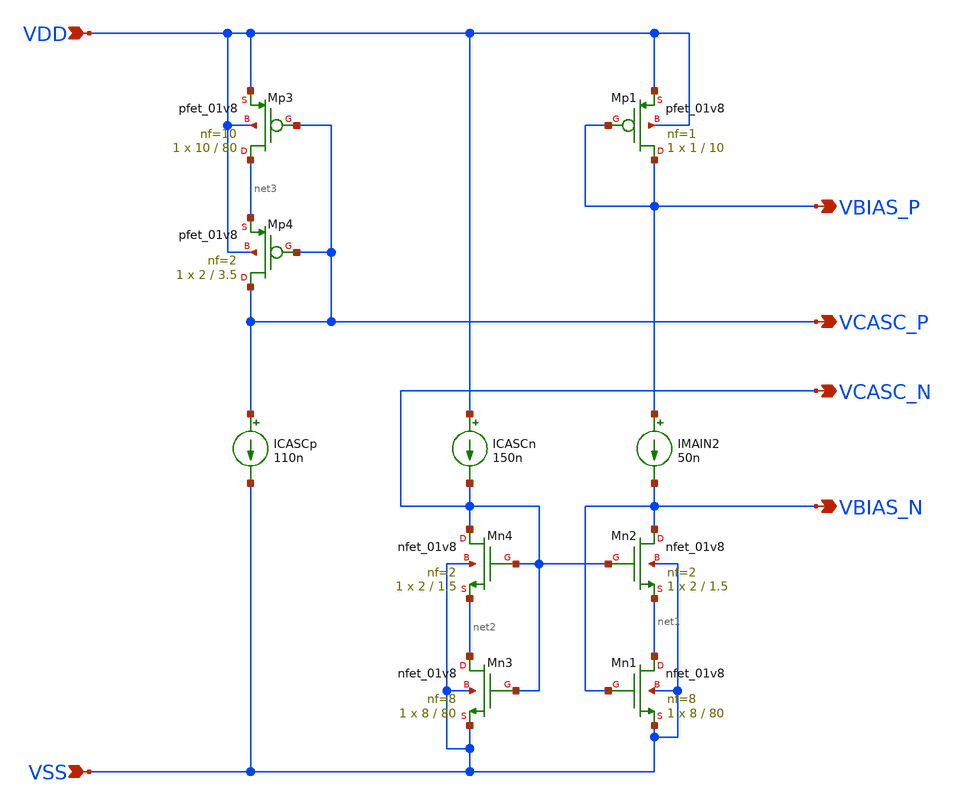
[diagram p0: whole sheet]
** sch_path: circuit-level/xschem/aux-amp/amp_gm_boost_bias_2.sch
**.subckt amp_gm_boost_bias_2 VBIAS_P VSS VDD VBIAS_N VCASC_N VCASC_P
*.opin VBIAS_P
*.ipin VSS
*.ipin VDD
*.opin VBIAS_N
*.opin VCASC_N
*.opin VCASC_P
XMn2 VBIAS_N VCASC_N net1 VSS sky130_fd_pr__nfet_01v8 L=1.5 W=2 nf=2 ad='int((nf+1)/2) * W/nf * 0.29'
+ as='int((nf+2)/2) * W/nf * 0.29' pd='2*int((nf+1)/2) * (W/nf + 0.29)' ps='2*int((nf+2)/2) * (W/nf + 0.29)'
+ nrd='0.29 / W' nrs='0.29 / W' sa=0 sb=0 sd=0 mult=1 m=1
XMn4 VCASC_N VCASC_N net2 VSS sky130_fd_pr__nfet_01v8 L=1.5 W=2 nf=2 ad='int((nf+1)/2) * W/nf * 0.29'
+ as='int((nf+2)/2) * W/nf * 0.29' pd='2*int((nf+1)/2) * (W/nf + 0.29)' ps='2*int((nf+2)/2) * (W/nf + 0.29)'
+ nrd='0.29 / W' nrs='0.29 / W' sa=0 sb=0 sd=0 mult=1 m=1
ICASCn VDD VCASC_N 150n
XMn1 net1 VBIAS_N VSS VSS sky130_fd_pr__nfet_01v8 L=80 W=8 nf=8 ad='int((nf+1)/2) * W/nf * 0.29' as='int((nf+2)/2) * W/nf * 0.29'
+ pd='2*int((nf+1)/2) * (W/nf + 0.29)' ps='2*int((nf+2)/2) * (W/nf + 0.29)' nrd='0.29 / W' nrs='0.29 / W'
+ sa=0 sb=0 sd=0 mult=1 m=1
IMAIN2 VBIAS_P VBIAS_N 50n
XMn3 net2 VCASC_N VSS VSS sky130_fd_pr__nfet_01v8 L=80 W=8 nf=8 ad='int((nf+1)/2) * W/nf * 0.29' as='int((nf+2)/2) * W/nf * 0.29'
+ pd='2*int((nf+1)/2) * (W/nf + 0.29)' ps='2*int((nf+2)/2) * (W/nf + 0.29)' nrd='0.29 / W' nrs='0.29 / W'
+ sa=0 sb=0 sd=0 mult=1 m=1
XMp1 VBIAS_P VBIAS_P VDD VDD sky130_fd_pr__pfet_01v8 L=10 W=1 nf=1 ad='int((nf+1)/2) * W/nf * 0.29' as='int((nf+2)/2) * W/nf * 0.29'
+ pd='2*int((nf+1)/2) * (W/nf + 0.29)' ps='2*int((nf+2)/2) * (W/nf + 0.29)' nrd='0.29 / W' nrs='0.29 / W'
+ sa=0 sb=0 sd=0 mult=1 m=1
ICASCp VCASC_P VSS 110n
XMp3 net3 VCASC_P VDD VDD sky130_fd_pr__pfet_01v8 L=80 W=10 nf=10 ad='int((nf+1)/2) * W/nf * 0.29' as='int((nf+2)/2) * W/nf * 0.29'
+ pd='2*int((nf+1)/2) * (W/nf + 0.29)' ps='2*int((nf+2)/2) * (W/nf + 0.29)' nrd='0.29 / W' nrs='0.29 / W'
+ sa=0 sb=0 sd=0 mult=1 m=1
XMp4 VCASC_P VCASC_P net3 VDD sky130_fd_pr__pfet_01v8 L=3.5 W=2 nf=2 ad='int((nf+1)/2) * W/nf * 0.29'
+ as='int((nf+2)/2) * W/nf * 0.29' pd='2*int((nf+1)/2) * (W/nf + 0.29)' ps='2*int((nf+2)/2) * (W/nf + 0.29)'
+ nrd='0.29 / W' nrs='0.29 / W' sa=0 sb=0 sd=0 mult=1 m=1
**.ends
.end
